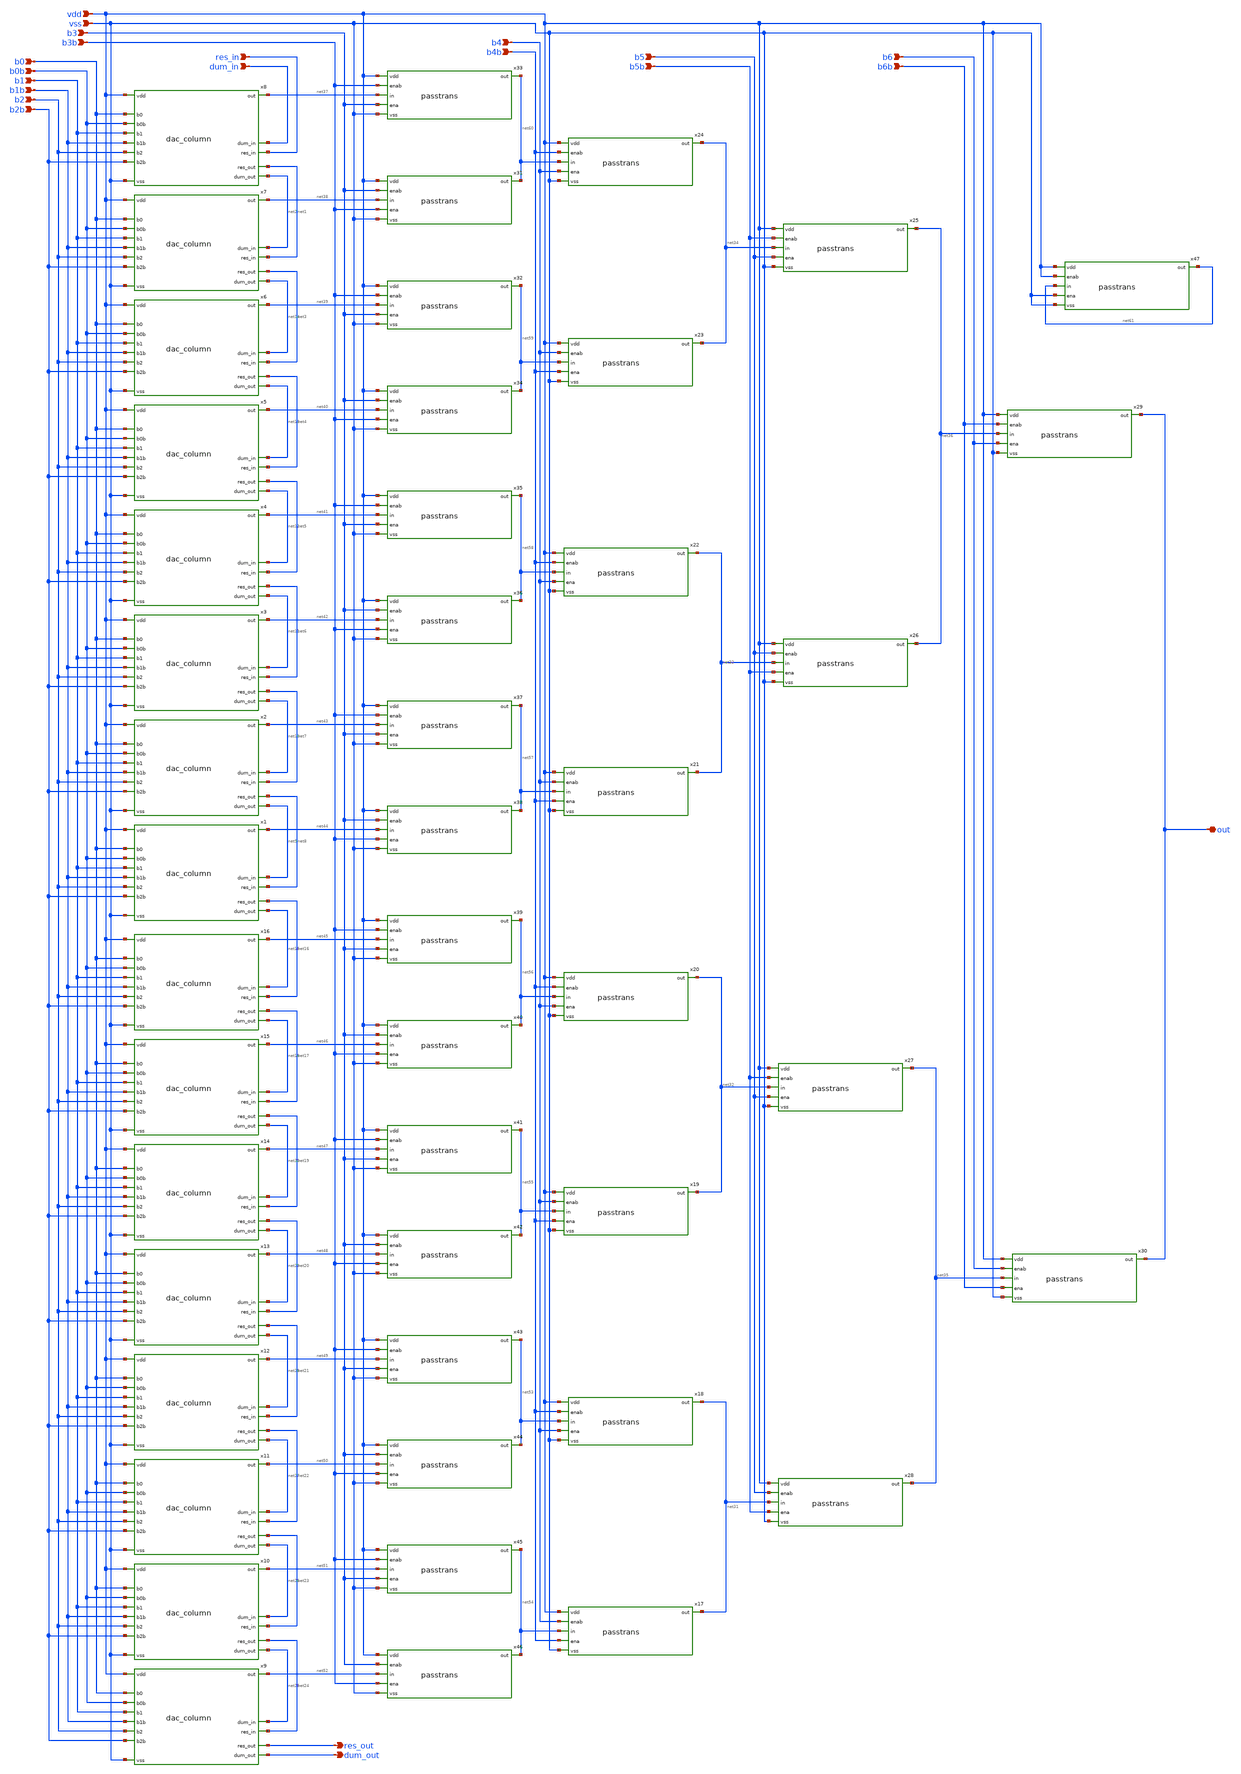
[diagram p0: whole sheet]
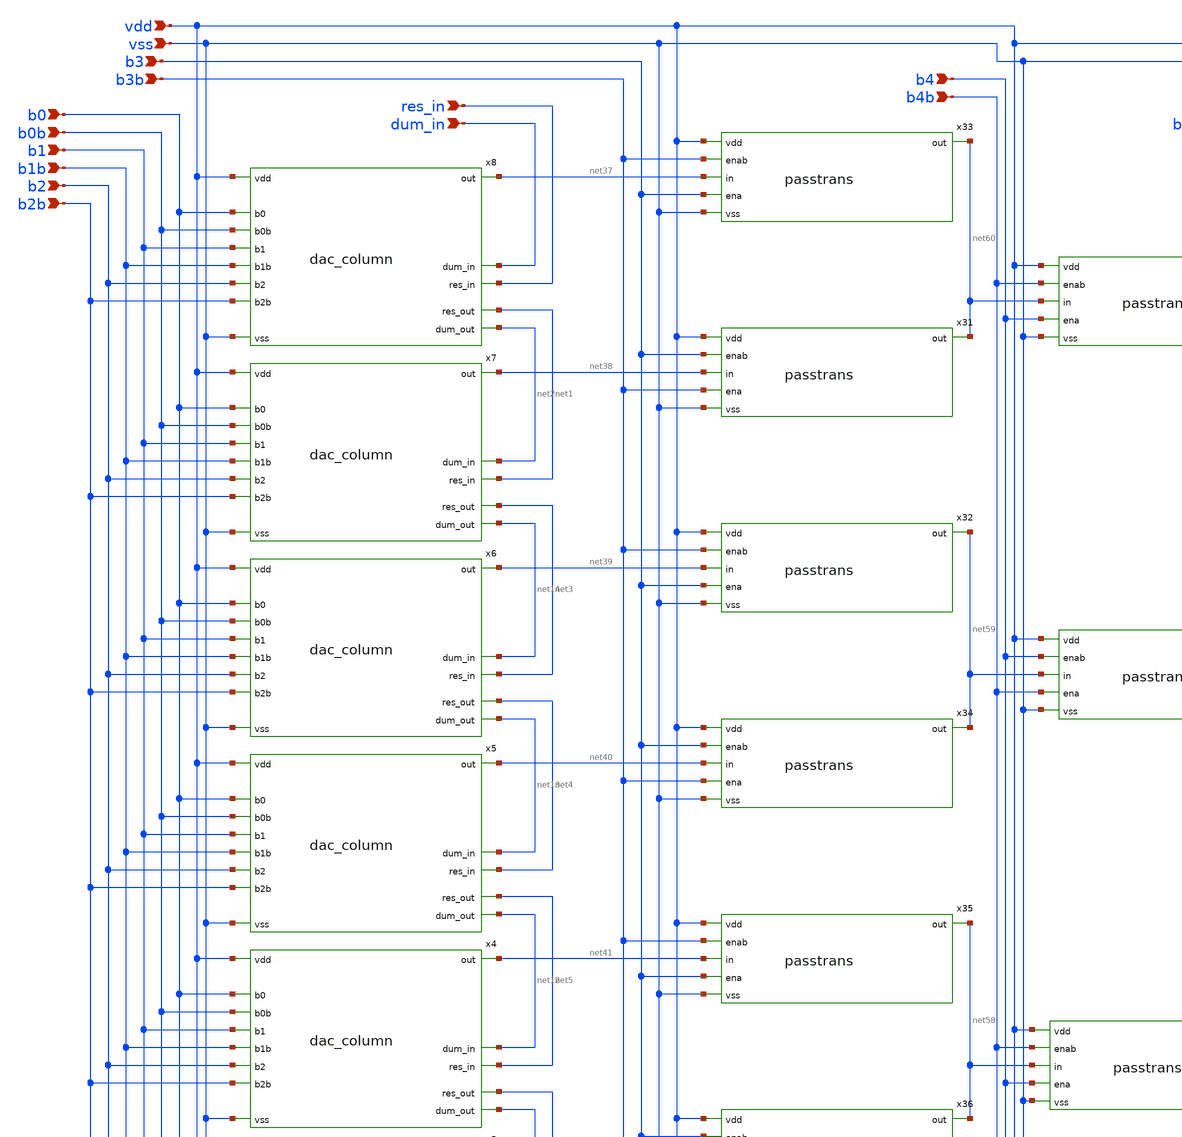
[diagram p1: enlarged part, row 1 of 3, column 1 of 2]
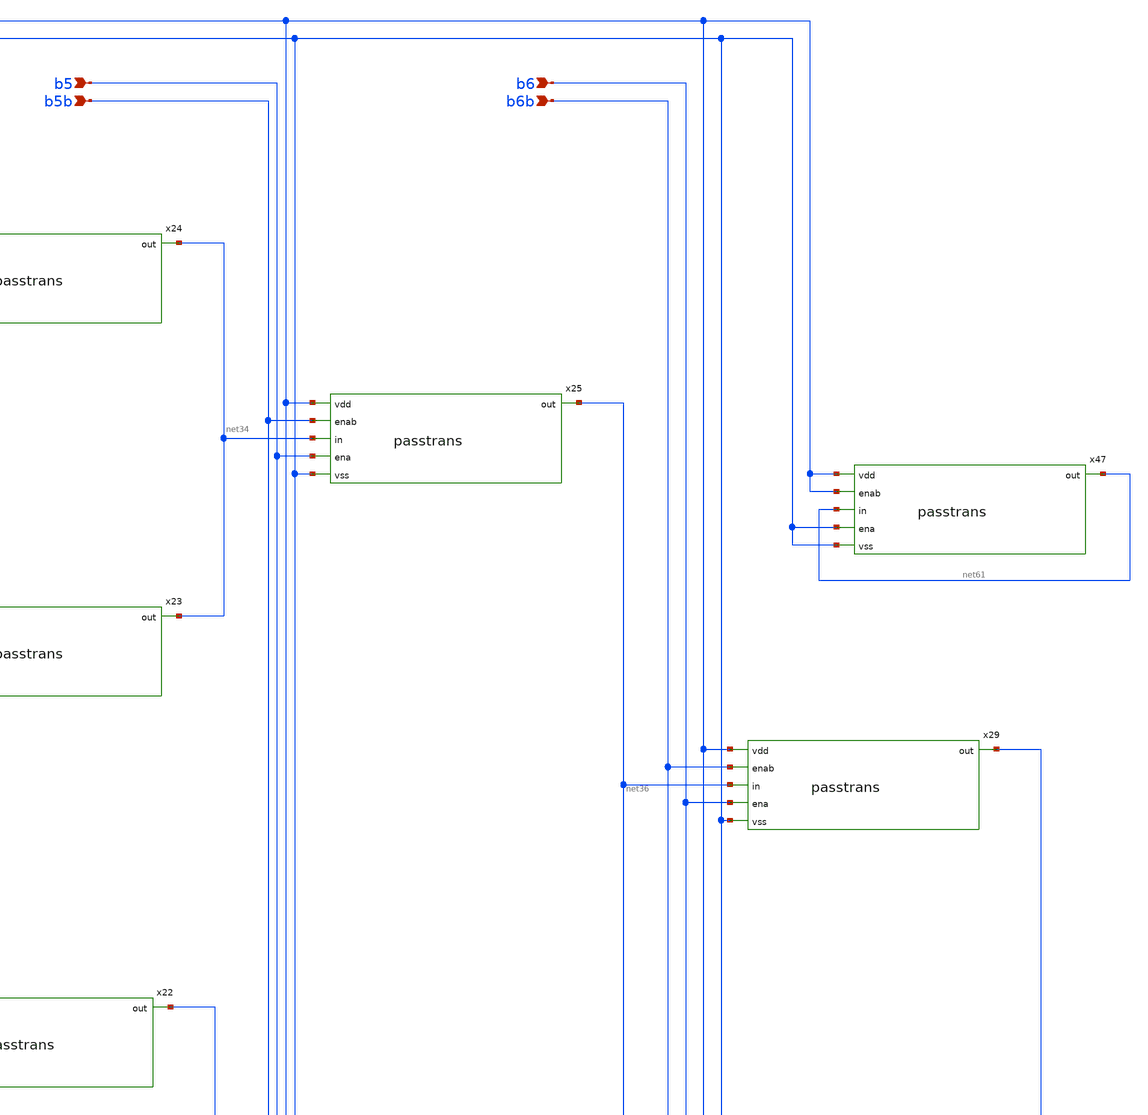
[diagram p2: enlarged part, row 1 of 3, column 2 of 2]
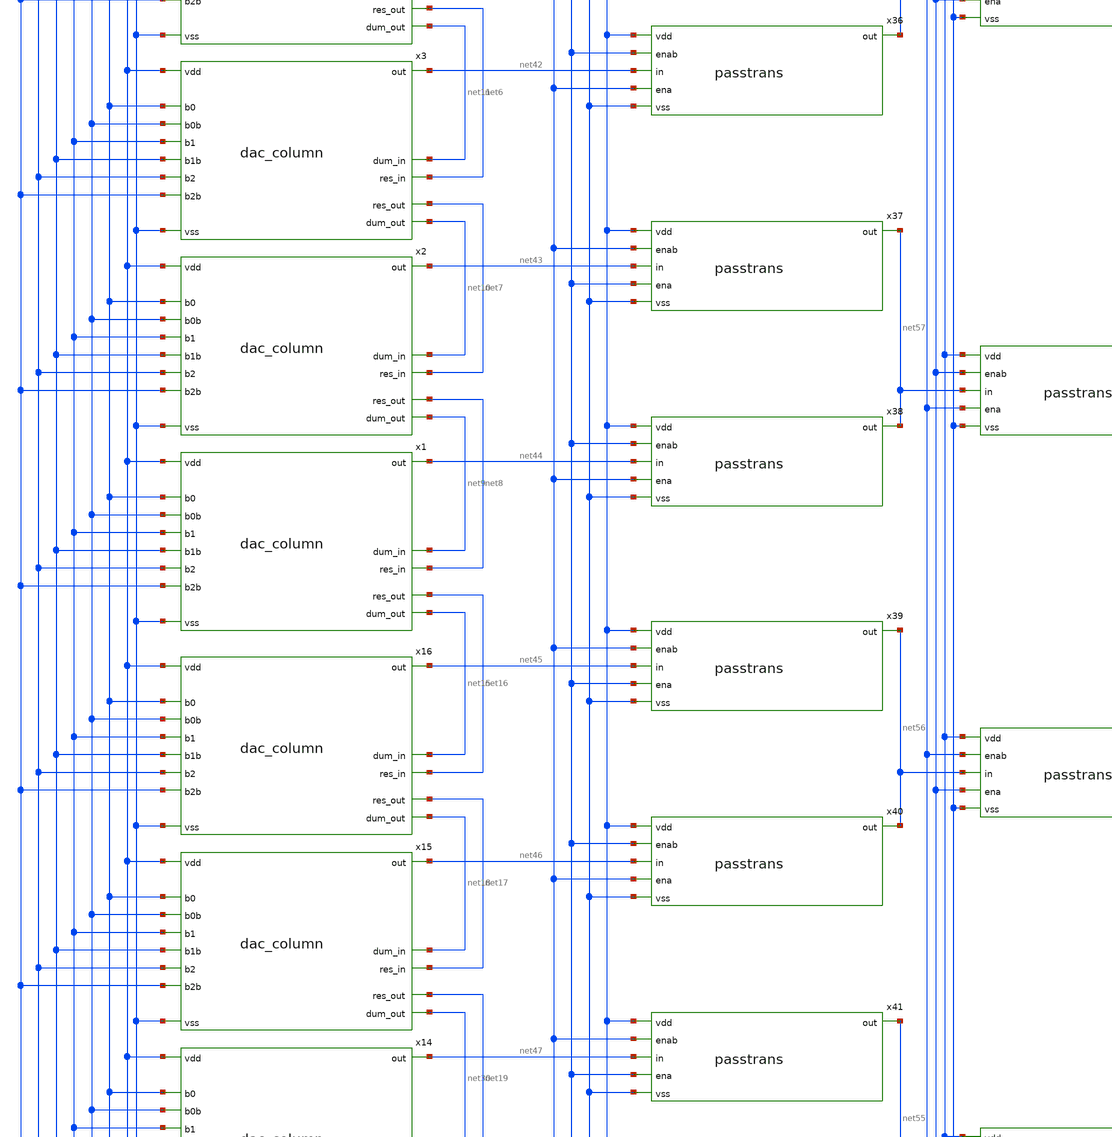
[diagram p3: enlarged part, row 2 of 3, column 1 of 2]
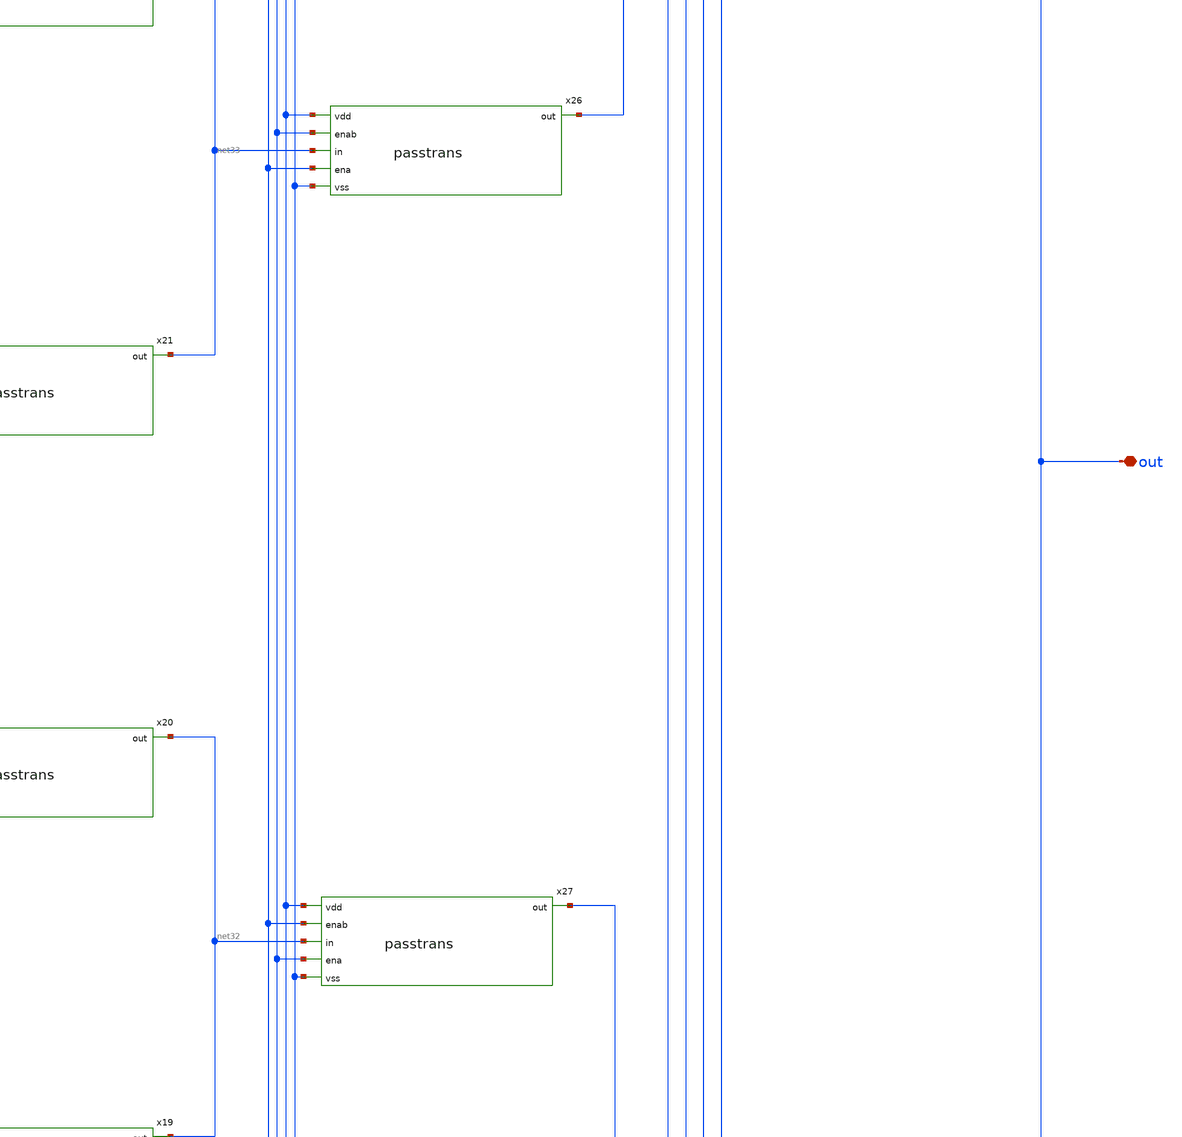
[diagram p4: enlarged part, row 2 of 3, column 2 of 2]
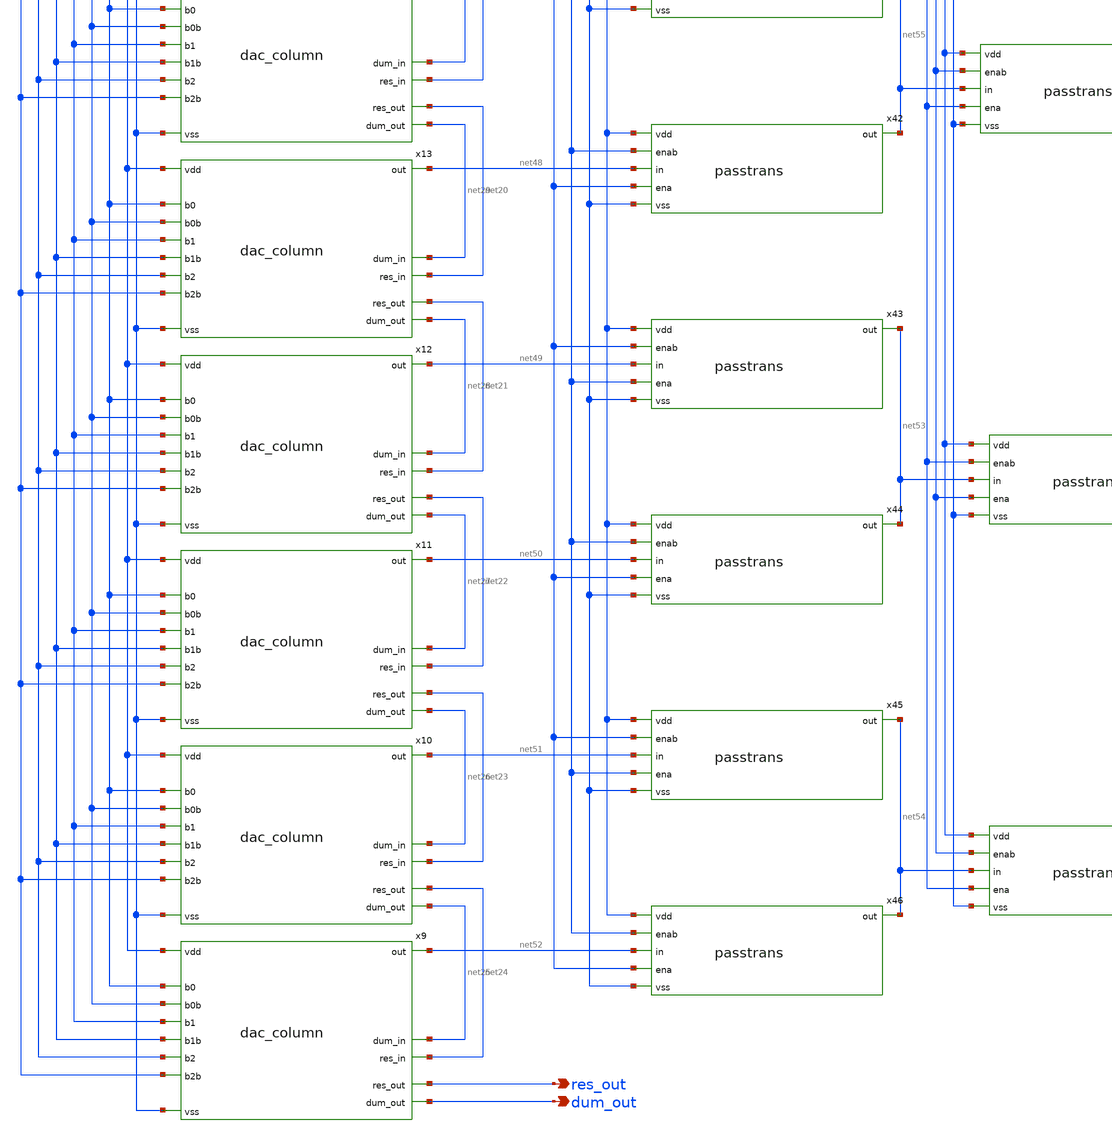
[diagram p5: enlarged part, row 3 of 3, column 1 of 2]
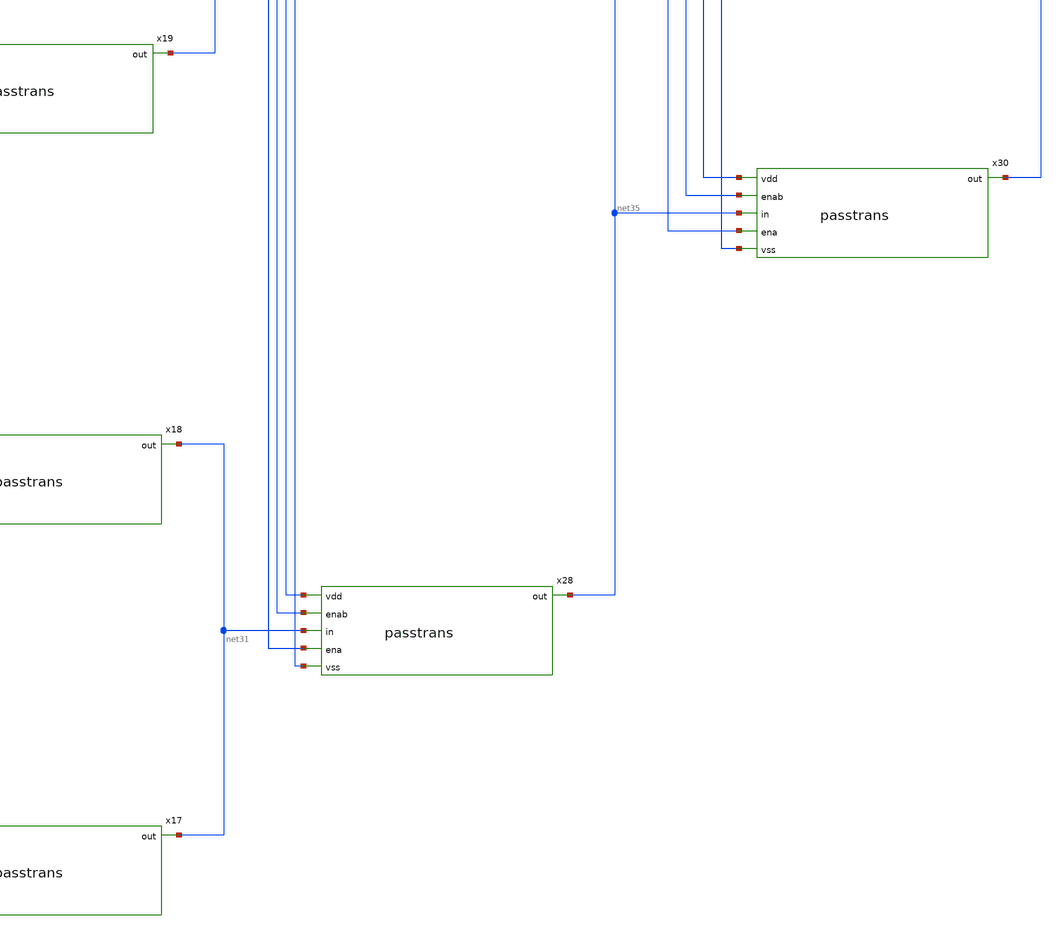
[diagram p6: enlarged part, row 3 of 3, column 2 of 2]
** sch_path: xschem/dac_half.sch
**.subckt dac_half res_in res_out out vdd vss b3 b3b b5 b5b b6 b6b dum_out dum_in b4 b4b b0 b0b b1
*+ b1b b2 b2b
*.ipin res_in
*.opin res_out
*.iopin out
*.ipin vdd
*.ipin vss
*.ipin b3
*.ipin b3b
*.ipin b5
*.ipin b5b
*.ipin b6
*.ipin b6b
*.opin dum_out
*.ipin dum_in
*.ipin b4
*.ipin b4b
*.ipin b0
*.ipin b0b
*.ipin b1
*.ipin b1b
*.ipin b2
*.ipin b2b
x1 b2 b2b b1 b1b b0 b0b vdd net9 net8 net44 net16 vss net15 dac_column
x2 b2 b2b b1 b1b b0 b0b vdd net10 net7 net43 net8 vss net9 dac_column
x3 b2 b2b b1 b1b b0 b0b vdd net11 net6 net42 net7 vss net10 dac_column
x4 b2 b2b b1 b1b b0 b0b vdd net12 net5 net41 net6 vss net11 dac_column
x5 b2 b2b b1 b1b b0 b0b vdd net13 net4 net40 net5 vss net12 dac_column
x6 b2 b2b b1 b1b b0 b0b vdd net14 net3 net39 net4 vss net13 dac_column
x7 b2 b2b b1 b1b b0 b0b vdd net2 net1 net38 net3 vss net14 dac_column
x8 b2 b2b b1 b1b b0 b0b vdd dum_in res_in net37 net1 vss net2 dac_column
x9 b2 b2b b1 b1b b0 b0b vdd net25 net24 net52 res_out vss dum_out dac_column
x10 b2 b2b b1 b1b b0 b0b vdd net26 net23 net51 net24 vss net25 dac_column
x11 b2 b2b b1 b1b b0 b0b vdd net27 net22 net50 net23 vss net26 dac_column
x12 b2 b2b b1 b1b b0 b0b vdd net28 net21 net49 net22 vss net27 dac_column
x13 b2 b2b b1 b1b b0 b0b vdd net29 net20 net48 net21 vss net28 dac_column
x14 b2 b2b b1 b1b b0 b0b vdd net30 net19 net47 net20 vss net29 dac_column
x15 b2 b2b b1 b1b b0 b0b vdd net18 net17 net46 net19 vss net30 dac_column
x16 b2 b2b b1 b1b b0 b0b vdd net15 net16 net45 net17 vss net18 dac_column
x17 vdd b4 net31 net54 b4b vss passtrans
x18 vdd b4b net31 net53 b4 vss passtrans
x19 vdd b4 net32 net55 b4b vss passtrans
x20 vdd b4b net32 net56 b4 vss passtrans
x21 vdd b4 net33 net57 b4b vss passtrans
x22 vdd b4b net33 net58 b4 vss passtrans
x23 vdd b4 net34 net59 b4b vss passtrans
x24 vdd b4b net34 net60 b4 vss passtrans
x25 vdd b5b net36 net34 b5 vss passtrans
x26 vdd b5 net36 net33 b5b vss passtrans
x27 vdd b5b net35 net32 b5 vss passtrans
x28 vdd b5 net35 net31 b5b vss passtrans
x29 vdd b6b out net36 b6 vss passtrans
x30 vdd b6 out net35 b6b vss passtrans
x33 vdd b3b net60 net37 b3 vss passtrans
x31 vdd b3 net60 net38 b3b vss passtrans
x32 vdd b3b net59 net39 b3 vss passtrans
x34 vdd b3 net59 net40 b3b vss passtrans
x35 vdd b3b net58 net41 b3 vss passtrans
x36 vdd b3 net58 net42 b3b vss passtrans
x37 vdd b3b net57 net43 b3 vss passtrans
x38 vdd b3 net57 net44 b3b vss passtrans
x39 vdd b3b net56 net45 b3 vss passtrans
x40 vdd b3 net56 net46 b3b vss passtrans
x41 vdd b3b net55 net47 b3 vss passtrans
x42 vdd b3 net55 net48 b3b vss passtrans
x43 vdd b3b net53 net49 b3 vss passtrans
x44 vdd b3 net53 net50 b3b vss passtrans
x45 vdd b3b net54 net51 b3 vss passtrans
x46 vdd b3 net54 net52 b3b vss passtrans
x47 vdd vdd net61 net61 vss vss passtrans
**.ends

* expanding   symbol:  dac_column.sym # of pins=13
** sym_path: xschem/dac_column.sym
** sch_path: xschem/dac_column.sch
.subckt dac_column b2 b2b b1 b1b b0 b0b vdd dum_in res_in out res_out vss dum_out
*.ipin res_in
*.ipin vss
*.ipin vdd
*.iopin out
*.ipin b0
*.ipin b0b
*.ipin b1
*.ipin b1b
*.ipin b2
*.ipin b2b
*.ipin dum_in
*.opin res_out
*.opin dum_out
x1 vdd b0 net8 net1 b0b vss passtrans
XR1 res_out net1 vss sky130_fd_pr__res_high_po_0p35 L=3 mult=1 m=1
x2 vdd b0b net8 net2 b0 vss passtrans
x3 vdd b0 net9 net3 b0b vss passtrans
x4 vdd b0b net9 net4 b0 vss passtrans
x5 vdd b0 net10 net5 b0b vss passtrans
x6 vdd b0b net10 net6 b0 vss passtrans
x7 vdd b0 net11 net7 b0b vss passtrans
x8 vdd b0b net11 res_in b0 vss passtrans
x9 vdd vdd net15 dum_in vss vss passtrans
x10 vdd vdd net12 res_out vss vss passtrans
XR2 net1 net2 vss sky130_fd_pr__res_high_po_0p35 L=3 mult=1 m=1
XR3 net2 net3 vss sky130_fd_pr__res_high_po_0p35 L=3 mult=1 m=1
XR4 net3 net4 vss sky130_fd_pr__res_high_po_0p35 L=3 mult=1 m=1
XR5 net4 net5 vss sky130_fd_pr__res_high_po_0p35 L=3 mult=1 m=1
XR6 net5 net6 vss sky130_fd_pr__res_high_po_0p35 L=3 mult=1 m=1
XR7 net6 net7 vss sky130_fd_pr__res_high_po_0p35 L=3 mult=1 m=1
XR8 net7 res_in vss sky130_fd_pr__res_high_po_0p35 L=3 mult=1 m=1
XR9 net7 res_in vss sky130_fd_pr__res_high_po_0p35 L=3 mult=1 m=1
XR10 res_in dum_in vss sky130_fd_pr__res_high_po_0p35 L=3 mult=1 m=1
XR12 dum_out res_out vss sky130_fd_pr__res_high_po_0p35 L=3 mult=1 m=1
x11 vdd b1b net14 net11 b1 vss passtrans
x12 vdd b1 net14 net10 b1b vss passtrans
x13 vdd b1b net13 net9 b1 vss passtrans
x14 vdd b1 net13 net8 b1b vss passtrans
x15 vdd b2b out net14 b2 vss passtrans
x16 vdd b2 out net13 b2b vss passtrans
x17 vdd vdd net15 net15 vss vss passtrans
x18 vdd vdd net12 net12 vss vss passtrans
.ends


* expanding   symbol:  passtrans.sym # of pins=6
** sym_path: xschem/passtrans.sym
** sch_path: xschem/passtrans.sch
.subckt passtrans vdd enab out in ena vss
*.ipin enab
*.ipin ena
*.ipin vss
*.ipin vdd
*.ipin in
*.iopin out
XM1 in ena out vss sky130_fd_pr__nfet_g5v0d10v5 L=0.5 W=0.65 nf=1 ad='int((nf+1)/2) * W/nf * 0.29' as='int((nf+2)/2) * W/nf * 0.29'
+ pd='2*int((nf+1)/2) * (W/nf + 0.29)' ps='2*int((nf+2)/2) * (W/nf + 0.29)' nrd='0.29 / W' nrs='0.29 / W'
+ sa=0 sb=0 sd=0 mult=1 m=1
XM2 in enab out vdd sky130_fd_pr__pfet_g5v0d10v5 L=0.5 W=1 nf=1 ad='int((nf+1)/2) * W/nf * 0.29' as='int((nf+2)/2) * W/nf * 0.29'
+ pd='2*int((nf+1)/2) * (W/nf + 0.29)' ps='2*int((nf+2)/2) * (W/nf + 0.29)' nrd='0.29 / W' nrs='0.29 / W'
+ sa=0 sb=0 sd=0 mult=1 m=1
.ends

.end
